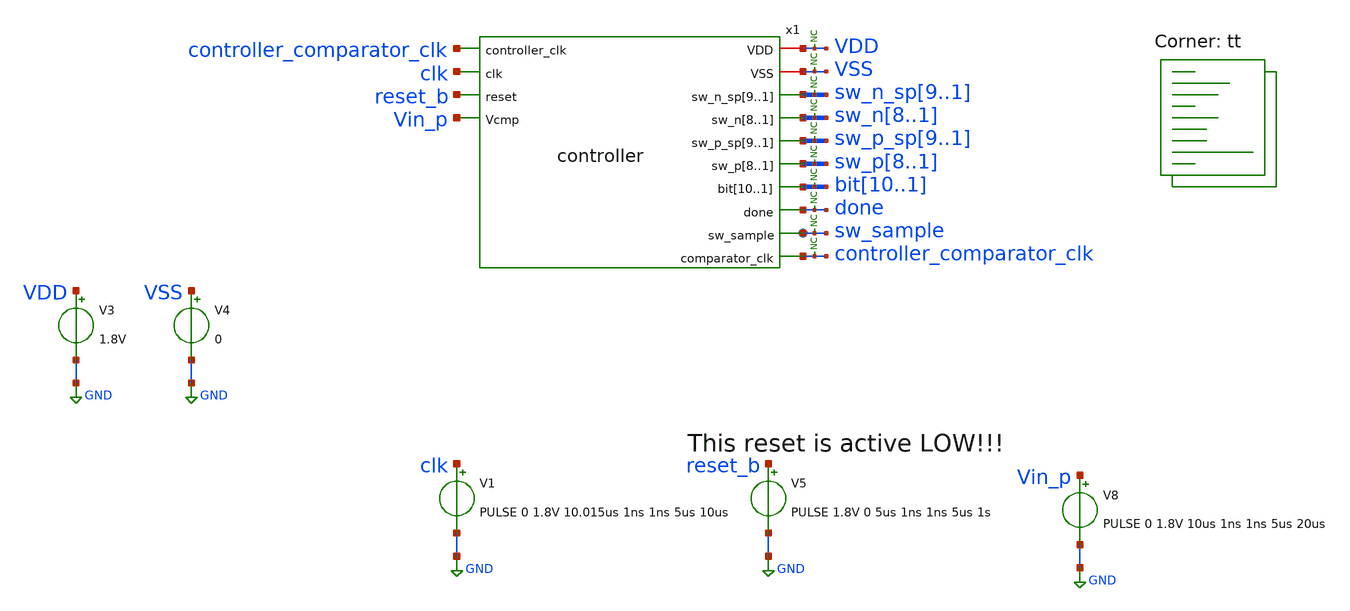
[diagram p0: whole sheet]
** sch_path: xschem/tests/controller/controller_test.sch
**.subckt controller_test
V3 VDD GND 1.8V
V4 VSS GND 0
x1 VDD controller_comparator_clk VSS sw_n_sp9 sw_n_sp8 sw_n_sp7 sw_n_sp6 sw_n_sp5 sw_n_sp4 sw_n_sp3
+ sw_n_sp2 sw_n_sp1 clk sw_n8 sw_n7 sw_n6 sw_n5 sw_n4 sw_n3 sw_n2 sw_n1 reset_b Vin_p sw_p_sp9 sw_p_sp8
+ sw_p_sp7 sw_p_sp6 sw_p_sp5 sw_p_sp4 sw_p_sp3 sw_p_sp2 sw_p_sp1 sw_p8 sw_p7 sw_p6 sw_p5 sw_p4 sw_p3 sw_p2
+ sw_p1 bit10 bit9 bit8 bit7 bit6 bit5 bit4 bit3 bit2 bit1 done sw_sample controller_comparator_clk
+ controller
V1 clk GND PULSE 0 1.8V 10.015us 1ns 1ns 5us 10us
V5 reset_b GND PULSE 1.8V 0 5us 1ns 1ns 5us 1s
V8 Vin_p GND PULSE 0 1.8V 10us 1ns 1ns 5us 20us
* noconn VDD
* noconn VSS
* noconn sw_n_sp[9..1]
* noconn sw_n[8..1]
* noconn sw_p_sp[9..1]
* noconn sw_p[8..1]
* noconn bit[10..1]
* noconn done
* noconn sw_sample
* noconn controller_comparator_clk
**** begin user architecture code
 *.lib $::SKYWATER_MODELS/sky130.lib.spice tt
.include $::SKYWATER_STDCELLS/sky130_fd_sc_hd.spice


.options acct list
.temp 25
*vvcc VDD 0 dc 1.8
*vvss VSS 0 0
.control
tran 0.1u 400u
*plot RST_PLS clk+2 Pulse+4
plot done-4  sw_n_sp1 sw_n_sp2+2 sw_n_sp3+4 sw_n_sp4+6 sw_n_sp5+8 sw_n_sp6+10 sw_n_sp7+12
+ sw_n_sp8+14 sw_n_sp9+16 Vin_p+18 clk+20
plot done-4  sw_p_sp1 sw_p_sp2+2 sw_p_sp3+4 sw_p_sp4+6 sw_p_sp5+8 sw_p_sp6+10 sw_p_sp7+12
+ sw_p_sp8+14 sw_p_sp9+16 Vin_p+18 clk+20
plot done-4  sw_n1 sw_n2+2 sw_n3+4 sw_n4+6 sw_n5+8 sw_n6+10 sw_n7+12 sw_n8+14 Vin_p+16 clk+18
plot done-4  sw_p1 sw_p2+2 sw_p3+4 sw_p4+6 sw_p5+8 sw_p6+10 sw_p7+12 sw_p8+14 Vin_p+16 clk+18
plot done-4 bit1 bit2+2 bit3+4 bit4+6 bit5+8 bit6+10 bit7+12 bit8+14 bit9+16 bit10+18

plot done-4  sw_n_sp1 sw_n_sp2+2 sw_n_sp3+4 sw_n_sp4+6 sw_n_sp5+8 sw_n_sp6+10 sw_n_sp7+12
+ sw_n_sp8+14 sw_n_sp9+16 Vin_q+18 clk+20 sw_n1 sw_n2+2 sw_n3+4 sw_n4+6 sw_n5+8 sw_n6+10 sw_n7+12 sw_n8+14

plot done-4  sw_p_sp1 sw_p_sp2+2 sw_p_sp3+4 sw_p_sp4+6 sw_p_sp5+8 sw_p_sp6+10 sw_p_sp7+12
+ sw_p_sp8+14 sw_p_sp9+16 Vin_q+18 clk+20 sw_p1 sw_p2+2 sw_p3+4 sw_p4+6 sw_p5+8 sw_p6+10 sw_p7+12 sw_p8+14

plot clk reset_b+2 x1.cycle0+4 x1.cycle1+6 x1.cycle2+8 x1.cycle16+10 x1.cycle17+12 x1.cycle18+14
+ sw_sample+16 vin_p+18

plot reset_b-2 clk vin_p gen_clk

write controller_test.raw
.endc


.lib $::SKYWATER_MODELS/sky130.lib.spice tt
**** end user architecture code
**.ends

* expanding   symbol:  src/controller/controller.sym # of pins=14
** sym_path: xschem/src/controller/controller.sym
** sch_path: xschem/src/controller/controller.sch
.subckt controller VDD controller_clk VSS sw_n_sp9 sw_n_sp8 sw_n_sp7 sw_n_sp6 sw_n_sp5 sw_n_sp4
+ sw_n_sp3 sw_n_sp2 sw_n_sp1 clk sw_n8 sw_n7 sw_n6 sw_n5 sw_n4 sw_n3 sw_n2 sw_n1 reset Vcmp sw_p_sp9 sw_p_sp8
+ sw_p_sp7 sw_p_sp6 sw_p_sp5 sw_p_sp4 sw_p_sp3 sw_p_sp2 sw_p_sp1 sw_p8 sw_p7 sw_p6 sw_p5 sw_p4 sw_p3 sw_p2
+ sw_p1 bit10 bit9 bit8 bit7 bit6 bit5 bit4 bit3 bit2 bit1 done sw_sample comparator_clk
*.ipin clk
*.opin sw_n_sp9,sw_n_sp8,sw_n_sp7,sw_n_sp6,sw_n_sp5,sw_n_sp4,sw_n_sp3,sw_n_sp2,sw_n_sp1
*.iopin VSS
*.iopin VDD
*.ipin reset
*.ipin Vcmp
*.opin sw_n8,sw_n7,sw_n6,sw_n5,sw_n4,sw_n3,sw_n2,sw_n1
*.opin sw_p_sp9,sw_p_sp8,sw_p_sp7,sw_p_sp6,sw_p_sp5,sw_p_sp4,sw_p_sp3,sw_p_sp2,sw_p_sp1
*.opin sw_p8,sw_p7,sw_p6,sw_p5,sw_p4,sw_p3,sw_p2,sw_p1
*.opin bit10,bit9,bit8,bit7,bit6,bit5,bit4,bit3,bit2,bit1
*.opin done
*.opin sw_sample
*.ipin controller_clk
*.opin comparator_clk
x3 VDD raw_bit13 raw_bit12 raw_bit11 raw_bit10 raw_bit9 raw_bit8 raw_bit7 raw_bit6 raw_bit5 raw_bit4
+ raw_bit3 raw_bit2 raw_bit1 VSS reset bit10 bit9 bit8 bit7 bit6 bit5 bit4 bit3 bit2 bit1 done cycle13 dec
x4 raw_bit13 raw_bit12 raw_bit11 raw_bit10 raw_bit9 raw_bit8 raw_bit7 raw_bit6 raw_bit5 raw_bit4
+ raw_bit3 raw_bit2 raw_bit1 cycle12 cycle11 cycle10 cycle9 cycle8 cycle7 cycle6 cycle5 cycle4 cycle3 cycle2
+ cycle1 cycle0 sw_p8 sw_p7 sw_p6 sw_p5 sw_p4 sw_p3 sw_p2 sw_p1 Vcmp_buff net7 VDD VSS sw_n_sp9 sw_n_sp8
+ sw_n_sp7 sw_n_sp6 sw_n_sp5 sw_n_sp4 sw_n_sp3 sw_n_sp2 sw_n_sp1 sw_n8 sw_n7 sw_n6 sw_n5 sw_n4 sw_n3 sw_n2
+ sw_n1 sw_p_sp9 sw_p_sp8 sw_p_sp7 sw_p_sp6 sw_p_sp5 sw_p_sp4 sw_p_sp3 sw_p_sp2 sw_p_sp1 raw_bit_calculator
x1 controller_clk VDD VSS reset cycle15 cycle14 cycle13 cycle12 cycle11 cycle10 cycle9 cycle8 cycle7
+ cycle6 cycle5 cycle4 cycle3 cycle2 cycle1 cycle0 shifted_clock_generator
x2 net1 reset VSS VSS VDD VDD net6 sky130_fd_sc_hd__and2_1
x6 cycle14 cycle15 VSS VSS VDD VDD net1 sky130_fd_sc_hd__xnor2_1
x25 net3 VSS VSS VDD VDD Vcmp_buff sky130_fd_sc_hd__buf_16
x26 Vcmp VSS VSS VDD VDD net2 sky130_fd_sc_hd__buf_4
x27 net2 VSS VSS VDD VDD net3 sky130_fd_sc_hd__buf_8
x28 net4 VSS VSS VDD VDD net7 sky130_fd_sc_hd__buf_16
x29 net6 VSS VSS VDD VDD net5 sky130_fd_sc_hd__buf_4
x30 net5 VSS VSS VDD VDD net4 sky130_fd_sc_hd__buf_8
x5 VDD clk reset VSS sw_sample comparator_clk sample_clock
x105 Vcmp_buff VSS VSS VDD VDD net8 sky130_fd_sc_hd__inv_1
x122 cycle0 Vcmp_buff reset VSS VSS VDD VDD test_sw_n1 sky130_fd_sc_hd__dfrtp_1
x7 cycle0 net8 reset VSS VSS VDD VDD test_sw_p1 sky130_fd_sc_hd__dfrtp_1
.ends


* expanding   symbol:  src/dec/dec.sym # of pins=7
** sym_path: xschem/src/dec/dec.sym
** sch_path: xschem/src/dec/dec.sch
.subckt dec VDD raw_bit13 raw_bit12 raw_bit11 raw_bit10 raw_bit9 raw_bit8 raw_bit7 raw_bit6 raw_bit5
+ raw_bit4 raw_bit3 raw_bit2 raw_bit1 VSS reset_b bit10 bit9 bit8 bit7 bit6 bit5 bit4 bit3 bit2 bit1 done
+ dump_bus
*.iopin VDD
*.iopin VSS
*.ipin reset_b
*.ipin dump_bus
*.opin done
*.ipin raw_bit13
*.ipin raw_bit12
*.ipin raw_bit11
*.ipin raw_bit10
*.ipin raw_bit9
*.ipin raw_bit8
*.ipin raw_bit7
*.ipin raw_bit6
*.ipin raw_bit5
*.ipin raw_bit4
*.ipin raw_bit3
*.ipin raw_bit2
*.ipin raw_bit1
*.opin bit10
*.opin bit9
*.opin bit8
*.opin bit7
*.opin bit6
*.opin bit5
*.opin bit4
*.opin bit3
*.opin bit2
*.opin bit1
x62 raw_bit2 raw_bit1 net1 VSS VSS VDD VDD net16 net2 sky130_fd_sc_hd__fa_1
x64 raw_bit3 raw_bit1 net4 VSS VSS VDD VDD net1 net3 sky130_fd_sc_hd__fa_1
x67 dump_bus net2 reset_b VSS VSS VDD VDD bit2 sky130_fd_sc_hd__dfrtp_1
x68 dump_bus net3 reset_b VSS VSS VDD VDD bit3 sky130_fd_sc_hd__dfrtp_1
x65 raw_bit5 raw_bit4 net5 VSS VSS VDD VDD net4 net6 sky130_fd_sc_hd__fa_1
x69 raw_bit6 raw_bit4 net8 VSS VSS VDD VDD net5 net7 sky130_fd_sc_hd__fa_1
x70 dump_bus net6 reset_b VSS VSS VDD VDD bit4 sky130_fd_sc_hd__dfrtp_1
x71 dump_bus net7 reset_b VSS VSS VDD VDD bit5 sky130_fd_sc_hd__dfrtp_1
x72 raw_bit7 raw_bit4 net9 VSS VSS VDD VDD net8 net10 sky130_fd_sc_hd__fa_1
x73 raw_bit9 raw_bit8 net12 VSS VSS VDD VDD net9 net11 sky130_fd_sc_hd__fa_1
x74 dump_bus net10 reset_b VSS VSS VDD VDD bit6 sky130_fd_sc_hd__dfrtp_1
x75 dump_bus net11 reset_b VSS VSS VDD VDD bit7 sky130_fd_sc_hd__dfrtp_1
x76 raw_bit10 raw_bit8 net13 VSS VSS VDD VDD net12 net14 sky130_fd_sc_hd__fa_1
x77 raw_bit11 raw_bit8 raw_bit12 VSS VSS VDD VDD net13 net15 sky130_fd_sc_hd__fa_1
x78 dump_bus net14 reset_b VSS VSS VDD VDD bit8 sky130_fd_sc_hd__dfrtp_1
x79 dump_bus net15 reset_b VSS VSS VDD VDD bit9 sky130_fd_sc_hd__dfrtp_1
x80 dump_bus net16 reset_b VSS VSS VDD VDD bit1 sky130_fd_sc_hd__dfrtp_1
x81 dump_bus raw_bit13 reset_b VSS VSS VDD VDD bit10 sky130_fd_sc_hd__dfrtp_1
x82 dump_bus VSS VSS VDD VDD done sky130_fd_sc_hd__inv_1
* noconn done
.ends


* expanding   symbol:  src/raw_bit_calculator/raw_bit_calculator.sym # of pins=10
** sym_path: xschem/src/raw_bit_calculator/raw_bit_calculator.sym
** sch_path: xschem/src/raw_bit_calculator/raw_bit_calculator.sch
.subckt raw_bit_calculator raw_bit13 raw_bit12 raw_bit11 raw_bit10 raw_bit9 raw_bit8 raw_bit7
+ raw_bit6 raw_bit5 raw_bit4 raw_bit3 raw_bit2 raw_bit1 cycle13 cycle12 cycle11 cycle10 cycle9 cycle8 cycle7
+ cycle6 cycle5 cycle4 cycle3 cycle2 cycle1 sw_p8 sw_p7 sw_p6 sw_p5 sw_p4 sw_p3 sw_p2 sw_p1 Vcmp RESET VDD
+ VSS sw_n_sp9 sw_n_sp8 sw_n_sp7 sw_n_sp6 sw_n_sp5 sw_n_sp4 sw_n_sp3 sw_n_sp2 sw_n_sp1 sw_n8 sw_n7 sw_n6
+ sw_n5 sw_n4 sw_n3 sw_n2 sw_n1 sw_p_sp9 sw_p_sp8 sw_p_sp7 sw_p_sp6 sw_p_sp5 sw_p_sp4 sw_p_sp3 sw_p_sp2
+ sw_p_sp1
*.ipin
*+ cycle13,cycle12,cycle11,cycle10,cycle9,cycle8,cycle7,cycle6,cycle5,cycle4,cycle3,cycle2,cycle1
*.opin sw_n_sp9,sw_n_sp8,sw_n_sp7,sw_n_sp6,sw_n_sp5,sw_n_sp4,sw_n_sp3,sw_n_sp2,sw_n_sp1
*.iopin VSS
*.iopin VDD
*.opin sw_n8,sw_n7,sw_n6,sw_n5,sw_n4,sw_n3,sw_n2,sw_n1
*.opin sw_p_sp9,sw_p_sp8,sw_p_sp7,sw_p_sp6,sw_p_sp5,sw_p_sp4,sw_p_sp3,sw_p_sp2,sw_p_sp1
*.opin sw_p8,sw_p7,sw_p6,sw_p5,sw_p4,sw_p3,sw_p2,sw_p1
*.ipin Vcmp
*.ipin RESET
*.opin
*+ raw_bit13,raw_bit12,raw_bit11,raw_bit10,raw_bit9,raw_bit8,raw_bit7,raw_bit6,raw_bit5,raw_bit4,raw_bit3,raw_bit2,raw_bit1
x29 raw_bit1 Vcmp VSS VSS VDD VDD net58 sky130_fd_sc_hd__xor2_1
x31 raw_bit1 Vcmp VSS VSS VDD VDD net62 sky130_fd_sc_hd__xor2_1
x37 raw_bit4 Vcmp VSS VSS VDD VDD net52 sky130_fd_sc_hd__xor2_1
x40 raw_bit4 Vcmp VSS VSS VDD VDD net53 sky130_fd_sc_hd__xor2_1
x45 raw_bit4 Vcmp VSS VSS VDD VDD net54 sky130_fd_sc_hd__xor2_1
x100 cycle1 net11 net23 VSS VSS VDD VDD sw_p_sp1 sky130_fd_sc_hd__dfrtp_1
x99 Vcmp VSS VSS VDD VDD net11 sky130_fd_sc_hd__inv_1
x102 cycle1 Vcmp net23 VSS VSS VDD VDD sw_n_sp1 sky130_fd_sc_hd__dfrtp_1
x25 cycle1 Vcmp net25 VSS VSS VDD VDD sw_n_sp2 sky130_fd_sc_hd__dfrtp_1
x103 Vcmp VSS VSS VDD VDD net12 sky130_fd_sc_hd__inv_1
x104 cycle1 net12 net25 VSS VSS VDD VDD sw_p_sp2 sky130_fd_sc_hd__dfrtp_1
x21 net1 Vcmp RESET VSS VSS VDD VDD sw_n1 sky130_fd_sc_hd__dfstp_1
x22 net1 net13 RESET VSS VSS VDD VDD sw_p1 sky130_fd_sc_hd__dfstp_1
x105 Vcmp VSS VSS VDD VDD net13 sky130_fd_sc_hd__inv_1
x28 net4 Vcmp RESET VSS VSS VDD VDD sw_n2 sky130_fd_sc_hd__dfstp_1
x106 net4 net14 RESET VSS VSS VDD VDD sw_p2 sky130_fd_sc_hd__dfstp_1
x107 Vcmp VSS VSS VDD VDD net14 sky130_fd_sc_hd__inv_1
x109 Vcmp VSS VSS VDD VDD net15 sky130_fd_sc_hd__inv_1
x111 Vcmp VSS VSS VDD VDD net16 sky130_fd_sc_hd__inv_1
x27 cycle4 Vcmp net27 VSS VSS VDD VDD sw_n_sp3 sky130_fd_sc_hd__dfrtp_1
x35 cycle4 net15 net27 VSS VSS VDD VDD sw_p_sp3 sky130_fd_sc_hd__dfrtp_1
x41 cycle4 Vcmp net28 VSS VSS VDD VDD sw_n_sp4 sky130_fd_sc_hd__dfrtp_1
x108 cycle4 net16 net28 VSS VSS VDD VDD sw_p_sp4 sky130_fd_sc_hd__dfrtp_1
x110 cycle4 Vcmp net29 VSS VSS VDD VDD sw_n_sp5 sky130_fd_sc_hd__dfrtp_1
x112 cycle4 net17 net29 VSS VSS VDD VDD sw_p_sp5 sky130_fd_sc_hd__dfrtp_1
x113 Vcmp VSS VSS VDD VDD net17 sky130_fd_sc_hd__inv_1
x114 net6 net18 RESET VSS VSS VDD VDD sw_p3 sky130_fd_sc_hd__dfstp_1
x32 net6 Vcmp RESET VSS VSS VDD VDD sw_n3 sky130_fd_sc_hd__dfstp_1
x115 Vcmp VSS VSS VDD VDD net18 sky130_fd_sc_hd__inv_1
x38 net7 Vcmp RESET VSS VSS VDD VDD sw_n4 sky130_fd_sc_hd__dfstp_1
x116 net7 net19 RESET VSS VSS VDD VDD sw_p4 sky130_fd_sc_hd__dfstp_1
x117 Vcmp VSS VSS VDD VDD net19 sky130_fd_sc_hd__inv_1
x43 net8 Vcmp RESET VSS VSS VDD VDD sw_n5 sky130_fd_sc_hd__dfstp_1
x118 net8 net20 RESET VSS VSS VDD VDD sw_p5 sky130_fd_sc_hd__dfstp_1
x119 Vcmp VSS VSS VDD VDD net20 sky130_fd_sc_hd__inv_1
x132 cycle12 net21 RESET VSS VSS VDD VDD sw_p_sp9 sky130_fd_sc_hd__dfrtp_1
x133 Vcmp VSS VSS VDD VDD net21 sky130_fd_sc_hd__inv_1
x61 cycle12 Vcmp RESET VSS VSS VDD VDD sw_n_sp9 sky130_fd_sc_hd__dfrtp_1
x24 net51 VDD VSS net1 net3 net2 demux2
x30 net61 VDD VSS net4 net60 net5 demux2
x34 net65 VDD VSS net6 net64 net22 demux2
x39 net68 VDD VSS net7 net67 net9 demux2
x44 net71 VDD VSS net8 net70 net10 demux2
x1 net2 VSS VSS VDD VDD net24 sky130_fd_sc_hd__inv_1
x2 net5 VSS VSS VDD VDD net26 sky130_fd_sc_hd__inv_1
x3 cycle1 Vcmp RESET VSS VSS VDD VDD raw_bit1 sky130_fd_sc_hd__dfrtp_4
x4 cycle2 Vcmp RESET VSS VSS VDD VDD raw_bit2 sky130_fd_sc_hd__dfrtp_4
x5 cycle3 Vcmp RESET VSS VSS VDD VDD raw_bit3 sky130_fd_sc_hd__dfrtp_4
x6 cycle4 Vcmp RESET VSS VSS VDD VDD raw_bit4 sky130_fd_sc_hd__dfrtp_4
x7 cycle5 Vcmp RESET VSS VSS VDD VDD raw_bit5 sky130_fd_sc_hd__dfrtp_4
x8 cycle6 Vcmp RESET VSS VSS VDD VDD raw_bit6 sky130_fd_sc_hd__dfrtp_4
x9 cycle7 Vcmp RESET VSS VSS VDD VDD raw_bit7 sky130_fd_sc_hd__dfrtp_4
x10 cycle8 Vcmp RESET VSS VSS VDD VDD raw_bit8 sky130_fd_sc_hd__dfrtp_4
x11 cycle9 Vcmp RESET VSS VSS VDD VDD raw_bit9 sky130_fd_sc_hd__dfrtp_4
x12 cycle10 Vcmp RESET VSS VSS VDD VDD raw_bit10 sky130_fd_sc_hd__dfrtp_4
x13 cycle11 Vcmp RESET VSS VSS VDD VDD raw_bit11 sky130_fd_sc_hd__dfrtp_4
x14 cycle12 Vcmp RESET VSS VSS VDD VDD raw_bit12 sky130_fd_sc_hd__dfrtp_4
x15 cycle13 Vcmp RESET VSS VSS VDD VDD raw_bit13 sky130_fd_sc_hd__dfrtp_4
x18 net22 VSS VSS VDD VDD net30 sky130_fd_sc_hd__inv_1
x19 net9 VSS VSS VDD VDD net31 sky130_fd_sc_hd__inv_1
x20 net10 VSS VSS VDD VDD net32 sky130_fd_sc_hd__inv_1
x42 raw_bit8 Vcmp VSS VSS VDD VDD net55 sky130_fd_sc_hd__xor2_1
x62 raw_bit8 Vcmp VSS VSS VDD VDD net56 sky130_fd_sc_hd__xor2_1
x64 raw_bit8 Vcmp VSS VSS VDD VDD net57 sky130_fd_sc_hd__xor2_1
x65 Vcmp VSS VSS VDD VDD net38 sky130_fd_sc_hd__inv_1
x66 Vcmp VSS VSS VDD VDD net39 sky130_fd_sc_hd__inv_1
x67 cycle8 Vcmp net45 VSS VSS VDD VDD sw_n_sp6 sky130_fd_sc_hd__dfrtp_1
x68 cycle8 net38 net45 VSS VSS VDD VDD sw_p_sp6 sky130_fd_sc_hd__dfrtp_1
x69 cycle8 Vcmp net46 VSS VSS VDD VDD sw_n_sp7 sky130_fd_sc_hd__dfrtp_1
x70 cycle8 net39 net46 VSS VSS VDD VDD sw_p_sp7 sky130_fd_sc_hd__dfrtp_1
x71 cycle8 Vcmp net47 VSS VSS VDD VDD sw_n_sp8 sky130_fd_sc_hd__dfrtp_1
x72 cycle8 net40 net47 VSS VSS VDD VDD sw_p_sp8 sky130_fd_sc_hd__dfrtp_1
x73 Vcmp VSS VSS VDD VDD net40 sky130_fd_sc_hd__inv_1
x74 net33 net41 RESET VSS VSS VDD VDD sw_p6 sky130_fd_sc_hd__dfstp_1
x75 net33 Vcmp RESET VSS VSS VDD VDD sw_n6 sky130_fd_sc_hd__dfstp_1
x76 Vcmp VSS VSS VDD VDD net41 sky130_fd_sc_hd__inv_1
x77 net34 Vcmp RESET VSS VSS VDD VDD sw_n7 sky130_fd_sc_hd__dfstp_1
x78 net34 net42 RESET VSS VSS VDD VDD sw_p7 sky130_fd_sc_hd__dfstp_1
x79 Vcmp VSS VSS VDD VDD net42 sky130_fd_sc_hd__inv_1
x80 net35 Vcmp RESET VSS VSS VDD VDD sw_n8 sky130_fd_sc_hd__dfstp_1
x81 net35 net43 RESET VSS VSS VDD VDD sw_p8 sky130_fd_sc_hd__dfstp_1
x82 Vcmp VSS VSS VDD VDD net43 sky130_fd_sc_hd__inv_1
x83 net74 VDD VSS net33 net73 net44 demux2
x84 net77 VDD VSS net34 net76 net36 demux2
x85 net80 VDD VSS net35 net79 net37 demux2
x88 net44 VSS VSS VDD VDD net48 sky130_fd_sc_hd__inv_1
x89 net36 VSS VSS VDD VDD net49 sky130_fd_sc_hd__inv_1
x90 net37 VSS VSS VDD VDD net50 sky130_fd_sc_hd__inv_1
x46 net24 RESET VSS VSS VDD VDD net23 sky130_fd_sc_hd__and2_0
x23 net26 RESET VSS VSS VDD VDD net25 sky130_fd_sc_hd__and2_0
x26 net30 RESET VSS VSS VDD VDD net27 sky130_fd_sc_hd__and2_0
x16 net31 RESET VSS VSS VDD VDD net28 sky130_fd_sc_hd__and2_0
x17 net32 RESET VSS VSS VDD VDD net29 sky130_fd_sc_hd__and2_0
x33 net48 RESET VSS VSS VDD VDD net45 sky130_fd_sc_hd__and2_0
x36 net49 RESET VSS VSS VDD VDD net46 sky130_fd_sc_hd__and2_0
x47 net50 RESET VSS VSS VDD VDD net47 sky130_fd_sc_hd__and2_0
x48 cycle2 net58 RESET VSS VSS VDD VDD net51 sky130_fd_sc_hd__dfrtp_1
x49 net59 VSS VSS VDD VDD net3 sky130_fd_sc_hd__clkdlybuf4s50_1
x50 cycle2 VSS VSS VDD VDD net59 sky130_fd_sc_hd__clkdlybuf4s50_1
x51 cycle3 net62 RESET VSS VSS VDD VDD net61 sky130_fd_sc_hd__dfrtp_1
x52 net63 VSS VSS VDD VDD net60 sky130_fd_sc_hd__clkdlybuf4s50_1
x53 cycle3 VSS VSS VDD VDD net63 sky130_fd_sc_hd__clkdlybuf4s50_1
x54 cycle5 net52 RESET VSS VSS VDD VDD net65 sky130_fd_sc_hd__dfrtp_1
x55 net66 VSS VSS VDD VDD net64 sky130_fd_sc_hd__clkdlybuf4s50_1
x56 cycle5 VSS VSS VDD VDD net66 sky130_fd_sc_hd__clkdlybuf4s50_1
x57 cycle6 net53 RESET VSS VSS VDD VDD net68 sky130_fd_sc_hd__dfrtp_1
x58 net69 VSS VSS VDD VDD net67 sky130_fd_sc_hd__clkdlybuf4s50_1
x59 cycle6 VSS VSS VDD VDD net69 sky130_fd_sc_hd__clkdlybuf4s50_1
x60 cycle7 net54 RESET VSS VSS VDD VDD net71 sky130_fd_sc_hd__dfrtp_1
x63 net72 VSS VSS VDD VDD net70 sky130_fd_sc_hd__clkdlybuf4s50_1
x86 cycle7 VSS VSS VDD VDD net72 sky130_fd_sc_hd__clkdlybuf4s50_1
x87 cycle9 net55 RESET VSS VSS VDD VDD net74 sky130_fd_sc_hd__dfrtp_1
x91 net75 VSS VSS VDD VDD net73 sky130_fd_sc_hd__clkdlybuf4s50_1
x92 cycle9 VSS VSS VDD VDD net75 sky130_fd_sc_hd__clkdlybuf4s50_1
x93 cycle10 net56 RESET VSS VSS VDD VDD net77 sky130_fd_sc_hd__dfrtp_1
x94 net78 VSS VSS VDD VDD net76 sky130_fd_sc_hd__clkdlybuf4s50_1
x95 cycle10 VSS VSS VDD VDD net78 sky130_fd_sc_hd__clkdlybuf4s50_1
x96 cycle11 net57 RESET VSS VSS VDD VDD net80 sky130_fd_sc_hd__dfrtp_1
x97 net81 VSS VSS VDD VDD net79 sky130_fd_sc_hd__clkdlybuf4s50_1
x98 cycle11 VSS VSS VDD VDD net81 sky130_fd_sc_hd__clkdlybuf4s50_1
x121 Vcmp VSS VSS VDD VDD net82 sky130_fd_sc_hd__inv_1
x122 cycle1 Vcmp RESET VSS VSS VDD VDD test_sw_n1_raw sky130_fd_sc_hd__dfrtp_1
x101 cycle1 net82 RESET VSS VSS VDD VDD test_sw_p1_raw sky130_fd_sc_hd__dfrtp_1
.ends


* expanding   symbol:  src/shifted_clock_generator/shifted_clock_generator.sym # of pins=5
** sym_path: xschem/src/shifted_clock_generator/shifted_clock_generator.sym
** sch_path: xschem/src/shifted_clock_generator/shifted_clock_generator.sch
.subckt shifted_clock_generator clk VDD VSS reset cycle15 cycle14 cycle13 cycle12 cycle11 cycle10
+ cycle9 cycle8 cycle7 cycle6 cycle5 cycle4 cycle3 cycle2 cycle1 cycle0
*.opin
*+ cycle15,cycle14,cycle13,cycle12,cycle11,cycle10,cycle9,cycle8,cycle7,cycle6,cycle5,cycle4,cycle3,cycle2,cycle1,cycle0
*.iopin VSS
*.iopin VDD
*.ipin clk
*.ipin reset
x32 clk net2 reset_b VSS VSS VDD VDD cycle1 sky130_fd_sc_hd__dfrtp_1
x1 net1 cycle1 reset_b VSS VSS VDD VDD cycle2 sky130_fd_sc_hd__dfrtp_1
x2 clk cycle2 reset_b VSS VSS VDD VDD cycle3 sky130_fd_sc_hd__dfrtp_1
x3 clk cycle3 reset_b VSS VSS VDD VDD cycle4 sky130_fd_sc_hd__dfrtp_1
x4 clk cycle4 reset_b VSS VSS VDD VDD cycle5 sky130_fd_sc_hd__dfrtp_1
x5 clk cycle5 reset_b VSS VSS VDD VDD cycle6 sky130_fd_sc_hd__dfrtp_1
x6 clk cycle6 reset_b VSS VSS VDD VDD cycle7 sky130_fd_sc_hd__dfrtp_1
x7 clk cycle7 reset_b VSS VSS VDD VDD cycle8 sky130_fd_sc_hd__dfrtp_1
x8 clk cycle8 reset_b VSS VSS VDD VDD cycle9 sky130_fd_sc_hd__dfrtp_1
x9 clk cycle9 reset_b VSS VSS VDD VDD cycle10 sky130_fd_sc_hd__dfrtp_1
x10 clk cycle10 reset_b VSS VSS VDD VDD cycle11 sky130_fd_sc_hd__dfrtp_1
x11 clk cycle11 reset_b VSS VSS VDD VDD cycle12 sky130_fd_sc_hd__dfrtp_1
x12 clk cycle12 reset_b VSS VSS VDD VDD cycle13 sky130_fd_sc_hd__dfrtp_1
x13 clk cycle13 reset_b VSS VSS VDD VDD cycle14 sky130_fd_sc_hd__dfrtp_1
x14 clk cycle14 reset_b VSS VSS VDD VDD cycle15 sky130_fd_sc_hd__dfrtp_1
x31 clk VDD reset_b VSS VSS VDD VDD net2 sky130_fd_sc_hd__dfrtp_1
x37 net3 VSS VSS VDD VDD reset_b sky130_fd_sc_hd__buf_16
x35 reset_cycle reset VSS VSS VDD VDD net3 sky130_fd_sc_hd__and2_4
x34 net7 VSS VSS VDD VDD net8 sky130_fd_sc_hd__clkdlybuf4s50_1
x39 half_cycle net13 VSS VSS VDD VDD reset_cycle sky130_fd_sc_hd__xnor2_1
x36 net6 VSS VSS VDD VDD net7 sky130_fd_sc_hd__clkdlybuf4s50_1
x40 net5 VSS VSS VDD VDD net6 sky130_fd_sc_hd__clkdlybuf4s50_1
x41 net4 VSS VSS VDD VDD net5 sky130_fd_sc_hd__clkdlybuf4s50_1
x42 half_cycle VSS VSS VDD VDD net4 sky130_fd_sc_hd__clkdlybuf4s50_1
x38 net12 VSS VSS VDD VDD net13 sky130_fd_sc_hd__clkdlybuf4s50_1
x43 net11 VSS VSS VDD VDD net12 sky130_fd_sc_hd__clkdlybuf4s50_1
x44 net10 VSS VSS VDD VDD net11 sky130_fd_sc_hd__clkdlybuf4s50_1
x45 net9 VSS VSS VDD VDD net10 sky130_fd_sc_hd__clkdlybuf4s50_1
x46 net8 VSS VSS VDD VDD net9 sky130_fd_sc_hd__clkdlybuf4s50_1
x48 clk VSS VSS VDD VDD net1 sky130_fd_sc_hd__buf_1
x49 net14 cycle15 reset_b VSS VSS VDD VDD half_cycle sky130_fd_sc_hd__dfrtn_1
x50 clk VSS VSS VDD VDD net14 sky130_fd_sc_hd__buf_1
x15 net2 VSS VSS VDD VDD cycle0 sky130_fd_sc_hd__buf_1
.ends


* expanding   symbol:  src/sample_clock/sample_clock.sym # of pins=6
** sym_path: xschem/src/sample_clock/sample_clock.sym
** sch_path: xschem/src/sample_clock/sample_clock.sch
.subckt sample_clock VDD clk reset VSS sw_sample comparator_clk
*.iopin VDD
*.ipin clk
*.opin sw_sample
*.iopin VSS
*.opin comparator_clk
*.ipin reset
x5 clk johnson_counter_loop reset VSS VSS VDD VDD sw_sample sky130_fd_sc_hd__dfrtp_1
x7 clk sw_sample reset VSS VSS VDD VDD net1 sky130_fd_sc_hd__dfrtp_1
x8 clk net1 reset VSS VSS VDD VDD net2 sky130_fd_sc_hd__dfrtp_1
x9 clk net2 reset VSS VSS VDD VDD net3 sky130_fd_sc_hd__dfrtp_1
x10 clk net3 reset VSS VSS VDD VDD net4 sky130_fd_sc_hd__dfrtp_1
x11 clk net4 reset VSS VSS VDD VDD net5 sky130_fd_sc_hd__dfrtp_1
x12 clk net5 reset VSS VSS VDD VDD net6 sky130_fd_sc_hd__dfrtp_1
x13 clk net6 reset VSS VSS VDD VDD net7 sky130_fd_sc_hd__dfrtp_1
x14 clk net7 reset VSS VSS VDD VDD net8 sky130_fd_sc_hd__dfrtp_1
x15 clk net8 reset VSS VSS VDD VDD net9 sky130_fd_sc_hd__dfrtp_1
x16 clk net9 reset VSS VSS VDD VDD net10 sky130_fd_sc_hd__dfrtp_1
x17 clk net10 reset VSS VSS VDD VDD net11 sky130_fd_sc_hd__dfrtp_1
x18 clk net11 reset VSS VSS VDD VDD net12 sky130_fd_sc_hd__dfrtp_1
x19 clk net12 reset VSS VSS VDD VDD net13 sky130_fd_sc_hd__dfrtp_1
x20 clk net13 reset VSS VSS VDD VDD net14 sky130_fd_sc_hd__dfrtp_1
x21 clk net14 reset VSS VSS VDD VDD net15 sky130_fd_sc_hd__dfrtp_1
x22 net15 VSS VSS VDD VDD johnson_counter_loop sky130_fd_sc_hd__inv_1
x23 clk net16 VSS VSS VDD VDD net19 sky130_fd_sc_hd__and2_1
x24 sw_sample VSS VSS VDD VDD net16 sky130_fd_sc_hd__inv_1
x25 net18 VSS VSS VDD VDD comparator_clk sky130_fd_sc_hd__buf_16
x26 net20 VSS VSS VDD VDD net17 sky130_fd_sc_hd__buf_4
x27 net17 VSS VSS VDD VDD net18 sky130_fd_sc_hd__buf_8
x1 net19 VSS VSS VDD VDD net20 sky130_fd_sc_hd__buf_2
.ends


* expanding   symbol:  src/demux2/demux2.sym # of pins=6
** sym_path: xschem/src/demux2/demux2.sym
** sch_path: xschem/src/demux2/demux2.sch
.subckt demux2 S VDD VSS OUT_0 IN OUT_1
*.ipin S
*.opin OUT_0
*.ipin IN
*.opin OUT_1
*.iopin VDD
*.iopin VSS
x1 net1 IN VSS VSS VDD VDD OUT_0 sky130_fd_sc_hd__and2_0
x2 S IN VSS VSS VDD VDD OUT_1 sky130_fd_sc_hd__and2_0
x3 S VSS VSS VDD VDD net1 sky130_fd_sc_hd__inv_1
.ends

.GLOBAL GND
.end
